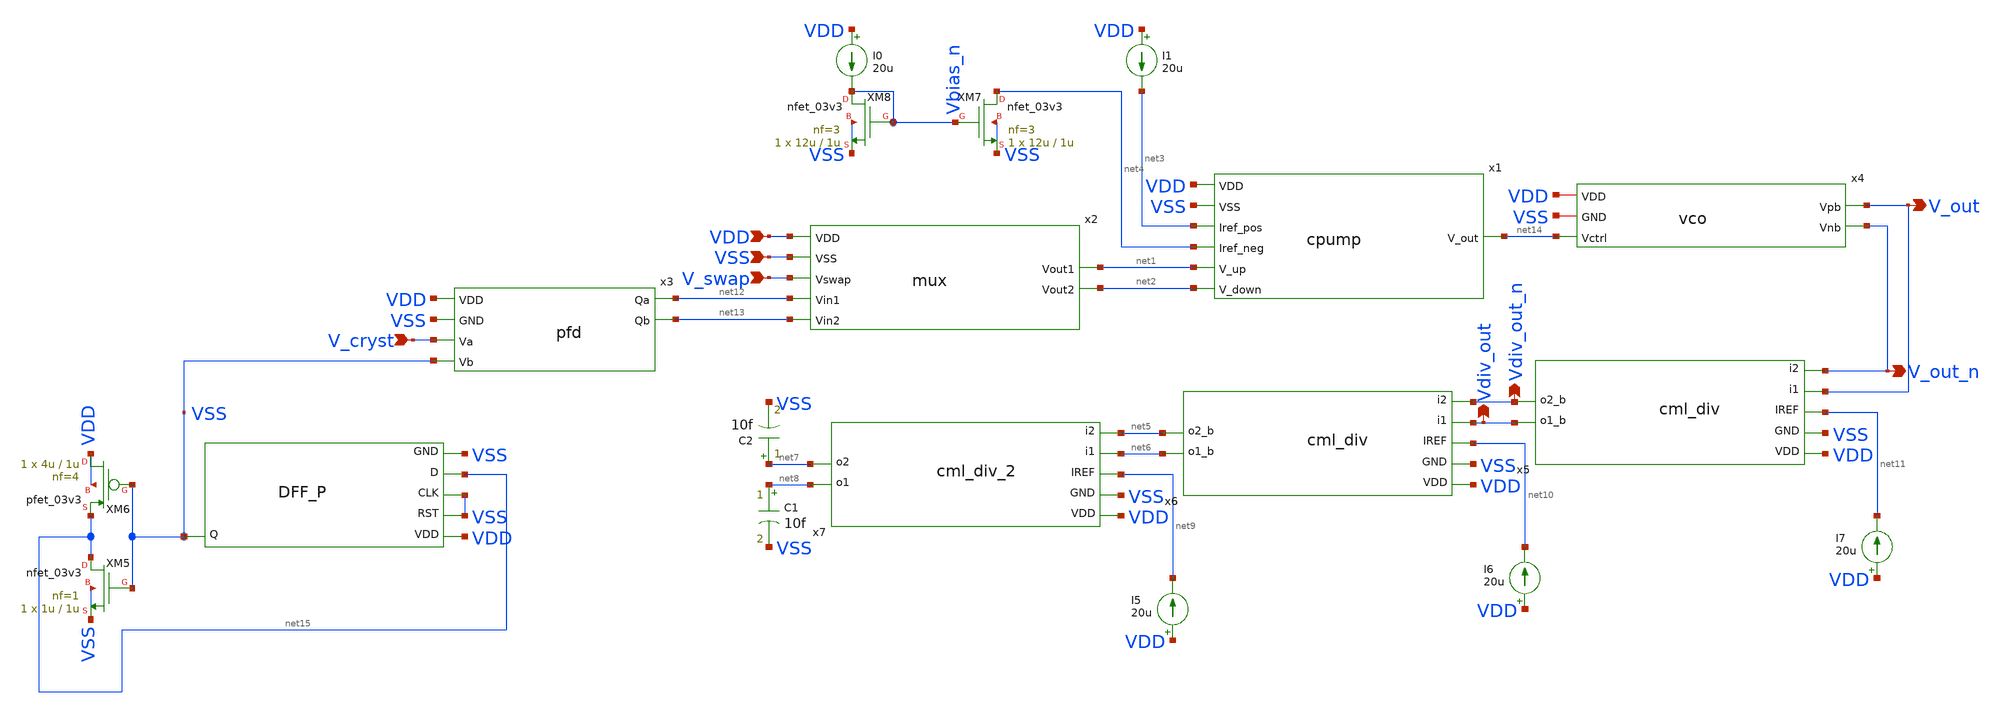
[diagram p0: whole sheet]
** sch_path: blocks/pll/pll.sch
**.subckt pll VDD VSS V_swap V_cryst V_out V_out_n Vdiv_out_n Vdiv_out
*.ipin VDD
*.ipin VSS
*.ipin V_swap
*.ipin V_cryst
*.opin V_out
*.opin V_out_n
*.opin Vdiv_out_n
*.opin Vdiv_out
x1 net3 VDD net1 net14 net2 VSS net4 cpump
x2 net2 net13 VDD V_swap VSS net1 net12 mux
x3 VDD VSS V_cryst net12 VSS net13 pfd
x4 V_out_n V_out net14 VDD VSS vco
x5 VDD VSS Vdiv_out Vdiv_out_n V_out_n V_out net11 cml_div
x6 VDD VSS net6 net5 Vdiv_out_n Vdiv_out net10 cml_div
XM7 net4 Vbias_n VSS VSS nfet_03v3 L=1u W=12u nf=3 ad='int((nf+1)/2) * W/nf * 0.18u' as='int((nf+2)/2) * W/nf * 0.18u'
+ pd='2*int((nf+1)/2) * (W/nf + 0.18u)' ps='2*int((nf+2)/2) * (W/nf + 0.18u)' nrd='0.18u / W' nrs='0.18u / W'
+ sa=0 sb=0 sd=0 m=1
XM8 Vbias_n Vbias_n VSS VSS nfet_03v3 L=1u W=12u nf=3 ad='int((nf+1)/2) * W/nf * 0.18u' as='int((nf+2)/2) * W/nf * 0.18u'
+ pd='2*int((nf+1)/2) * (W/nf + 0.18u)' ps='2*int((nf+2)/2) * (W/nf + 0.18u)' nrd='0.18u / W' nrs='0.18u / W'
+ sa=0 sb=0 sd=0 m=1
I0 VDD Vbias_n 20u
I1 VDD net3 20u
I5 VDD net9 20u
I6 VDD net10 20u
I7 VDD net11 20u
x8 VDD VSS VSS net15 VSS VSS dff_encoder
XM5 net15 VSS VSS VSS nfet_03v3 L=1u W=1u nf=1 ad='int((nf+1)/2) * W/nf * 0.18u' as='int((nf+2)/2) * W/nf * 0.18u'
+ pd='2*int((nf+1)/2) * (W/nf + 0.18u)' ps='2*int((nf+2)/2) * (W/nf + 0.18u)' nrd='0.18u / W' nrs='0.18u / W'
+ sa=0 sb=0 sd=0 m=1
XM6 VDD VSS net15 VDD pfet_03v3 L=1u W=4u nf=4 ad='int((nf+1)/2) * W/nf * 0.18u' as='int((nf+2)/2) * W/nf * 0.18u'
+ pd='2*int((nf+1)/2) * (W/nf + 0.18u)' ps='2*int((nf+2)/2) * (W/nf + 0.18u)' nrd='0.18u / W' nrs='0.18u / W'
+ sa=0 sb=0 sd=0 m=1
x7 VDD VSS net8 net7 net5 net6 net9 cml_div_2
C1 net8 VSS 10f m=1
C2 net7 VSS 10f m=1
**** begin user architecture code

.include /foss/pdks/gf180mcuD/libs.tech/ngspice/design.ngspice
.lib /foss/pdks/gf180mcuD/libs.tech/ngspice/sm141064.ngspice typical
.lib /foss/pdks/gf180mcuD/libs.tech/ngspice/sm141064.ngspice bjt_typical
.lib /foss/pdks/gf180mcuD/libs.tech/ngspice/sm141064.ngspice diode_typical
.lib /foss/pdks/gf180mcuD/libs.tech/ngspice/sm141064.ngspice res_typical
.lib /foss/pdks/gf180mcuD/libs.tech/ngspice/sm141064.ngspice mimcap_typical
.lib /foss/pdks/gf180mcuD/libs.tech/ngspice/sm141064.ngspice moscap_typical

.option method = gear

V_VDD   VDD     0 DC 3.3
V_VSS   VSS     0 DC 0
V_SWP   V_swap  0 DC 0
V_CRYST V_cryst 0 SIN(1.65 1.65 50meg 0 0 0)

.control
    set temp = 25

    let freq = 50meg
    let pers = 500
    let persteps = 20

    let tper = 1 / freq
    let tfin = tper * pers
    let tstep = tper / persteps
    let tplotst = tfin - 2 * tper

    tran 10ps 100ns
    write pll_toplevel.raw

    plot V_out xlimit $&tplotst $&tfin
.endc


**** end user architecture code
**.ends

* expanding   symbol:  blocks/pll/cpump.sym # of pins=7
** sym_path: blocks/pll/cpump.sym
** sch_path: blocks/pll/cpump.sch
.subckt cpump Iref_pos VDD V_up V_out V_down VSS Iref_neg
*.ipin Iref_pos
*.ipin Iref_neg
*.ipin V_up
*.ipin V_down
*.iopin VDD
*.iopin VSS
*.opin V_out
XM1 V_out V_up Iref_pos VDD pfet_03v3 L=1u W=40u nf=10 ad='int((nf+1)/2) * W/nf * 0.18u' as='int((nf+2)/2) * W/nf * 0.18u'
+ pd='2*int((nf+1)/2) * (W/nf + 0.18u)' ps='2*int((nf+2)/2) * (W/nf + 0.18u)' nrd='0.18u / W' nrs='0.18u / W'
+ sa=0 sb=0 sd=0 m=1
XM2 V_out V_down Iref_neg VSS nfet_03v3 L=1u W=4u nf=1 ad='int((nf+1)/2) * W/nf * 0.18u' as='int((nf+2)/2) * W/nf * 0.18u'
+ pd='2*int((nf+1)/2) * (W/nf + 0.18u)' ps='2*int((nf+2)/2) * (W/nf + 0.18u)' nrd='0.18u / W' nrs='0.18u / W'
+ sa=0 sb=0 sd=0 m=1
XR1 net1 V_out VSS ppolyf_u r_width=2e-6 r_length=8e-6 m=1
XC1 net1 VSS cap_mim_2f0_m4m5_noshield c_width=5e-6 c_length=5e-6 m=1
XC2 V_out VSS cap_mim_2f0_m4m5_noshield c_width=5e-6 c_length=5e-6 m=1
.ends


* expanding   symbol:  blocks/pll/mux.sym # of pins=7
** sym_path: blocks/pll/mux.sym
** sch_path: blocks/pll/mux.sch
.subckt mux Vout2 Vin2 VDD Vswap VSS Vout1 Vin1
*.ipin Vin1
*.opin Vout1
*.ipin Vin2
*.opin Vout2
*.iopin VDD
*.iopin VSS
*.ipin Vswap
XM1 Vout1 net1 Vin2 VSS nfet_03v3 L=1u W=4u nf=1 ad='int((nf+1)/2) * W/nf * 0.18u' as='int((nf+2)/2) * W/nf * 0.18u'
+ pd='2*int((nf+1)/2) * (W/nf + 0.18u)' ps='2*int((nf+2)/2) * (W/nf + 0.18u)' nrd='0.18u / W' nrs='0.18u / W'
+ sa=0 sb=0 sd=0 m=1
XM2 Vout1 Vswap Vin2 VDD pfet_03v3 L=1u W=16u nf=4 ad='int((nf+1)/2) * W/nf * 0.18u' as='int((nf+2)/2) * W/nf * 0.18u'
+ pd='2*int((nf+1)/2) * (W/nf + 0.18u)' ps='2*int((nf+2)/2) * (W/nf + 0.18u)' nrd='0.18u / W' nrs='0.18u / W'
+ sa=0 sb=0 sd=0 m=1
XM3 Vout2 Vswap Vin1 VSS nfet_03v3 L=1u W=4u nf=1 ad='int((nf+1)/2) * W/nf * 0.18u' as='int((nf+2)/2) * W/nf * 0.18u'
+ pd='2*int((nf+1)/2) * (W/nf + 0.18u)' ps='2*int((nf+2)/2) * (W/nf + 0.18u)' nrd='0.18u / W' nrs='0.18u / W'
+ sa=0 sb=0 sd=0 m=1
XM4 Vout2 net1 Vin1 VDD pfet_03v3 L=1u W=16u nf=4 ad='int((nf+1)/2) * W/nf * 0.18u' as='int((nf+2)/2) * W/nf * 0.18u'
+ pd='2*int((nf+1)/2) * (W/nf + 0.18u)' ps='2*int((nf+2)/2) * (W/nf + 0.18u)' nrd='0.18u / W' nrs='0.18u / W'
+ sa=0 sb=0 sd=0 m=1
XM5 net1 Vswap VSS VSS nfet_03v3 L=1u W=1u nf=1 ad='int((nf+1)/2) * W/nf * 0.18u' as='int((nf+2)/2) * W/nf * 0.18u'
+ pd='2*int((nf+1)/2) * (W/nf + 0.18u)' ps='2*int((nf+2)/2) * (W/nf + 0.18u)' nrd='0.18u / W' nrs='0.18u / W'
+ sa=0 sb=0 sd=0 m=1
XM6 VDD Vswap net1 VDD pfet_03v3 L=1u W=4u nf=4 ad='int((nf+1)/2) * W/nf * 0.18u' as='int((nf+2)/2) * W/nf * 0.18u'
+ pd='2*int((nf+1)/2) * (W/nf + 0.18u)' ps='2*int((nf+2)/2) * (W/nf + 0.18u)' nrd='0.18u / W' nrs='0.18u / W'
+ sa=0 sb=0 sd=0 m=1
XM7 Vout2 net1 Vin2 VSS nfet_03v3 L=1u W=4u nf=1 ad='int((nf+1)/2) * W/nf * 0.18u' as='int((nf+2)/2) * W/nf * 0.18u'
+ pd='2*int((nf+1)/2) * (W/nf + 0.18u)' ps='2*int((nf+2)/2) * (W/nf + 0.18u)' nrd='0.18u / W' nrs='0.18u / W'
+ sa=0 sb=0 sd=0 m=1
XM8 Vout2 Vswap Vin2 VDD pfet_03v3 L=1u W=16u nf=4 ad='int((nf+1)/2) * W/nf * 0.18u' as='int((nf+2)/2) * W/nf * 0.18u'
+ pd='2*int((nf+1)/2) * (W/nf + 0.18u)' ps='2*int((nf+2)/2) * (W/nf + 0.18u)' nrd='0.18u / W' nrs='0.18u / W'
+ sa=0 sb=0 sd=0 m=1
XM9 Vout1 Vswap Vin1 VSS nfet_03v3 L=1u W=4u nf=1 ad='int((nf+1)/2) * W/nf * 0.18u' as='int((nf+2)/2) * W/nf * 0.18u'
+ pd='2*int((nf+1)/2) * (W/nf + 0.18u)' ps='2*int((nf+2)/2) * (W/nf + 0.18u)' nrd='0.18u / W' nrs='0.18u / W'
+ sa=0 sb=0 sd=0 m=1
XM10 Vout1 net1 Vin1 VDD pfet_03v3 L=1u W=16u nf=4 ad='int((nf+1)/2) * W/nf * 0.18u' as='int((nf+2)/2) * W/nf * 0.18u'
+ pd='2*int((nf+1)/2) * (W/nf + 0.18u)' ps='2*int((nf+2)/2) * (W/nf + 0.18u)' nrd='0.18u / W' nrs='0.18u / W'
+ sa=0 sb=0 sd=0 m=1
.ends


* expanding   symbol:  blocks/pll/pfd.sym # of pins=6
** sym_path: pll_block_templates_v1/layout2/pfd.sym
** sch_path: pll_block_templates_v1/layout2/pfd.sch
.subckt pfd VDD GND Va Qa Vb Qb
*.ipin Vb
*.ipin Va
*.opin Qa
*.opin Qb
*.iopin VDD
*.iopin GND
x2 VDD Va Qa net1 GND nor
x3 VDD net1 net2 Qa GND nor
x4 VDD net1 net3 net2 GND nor
x5 VDD net2 RST net3 GND nor
x1 VDD Vb Qb net4 GND nor
x6 VDD net4 net5 Qb GND nor
x7 VDD net4 net6 net5 GND nor
x8 VDD net5 RST net6 GND nor
x9 VDD net7 Qa Qb GND nand
XM1 RST net7 GND GND nfet_03v3 L=0.28u W=0.22u nf=1 ad='int((nf+1)/2) * W/nf * 0.18u' as='int((nf+2)/2) * W/nf * 0.18u'
+ pd='2*int((nf+1)/2) * (W/nf + 0.18u)' ps='2*int((nf+2)/2) * (W/nf + 0.18u)' nrd='0.18u / W' nrs='0.18u / W'
+ sa=0 sb=0 sd=0 m=1
XM2 RST net7 VDD VDD pfet_03v3 L=0.28u W=0.22u nf=1 ad='int((nf+1)/2) * W/nf * 0.18u' as='int((nf+2)/2) * W/nf * 0.18u'
+ pd='2*int((nf+1)/2) * (W/nf + 0.18u)' ps='2*int((nf+2)/2) * (W/nf + 0.18u)' nrd='0.18u / W' nrs='0.18u / W'
+ sa=0 sb=0 sd=0 m=1
.ends


* expanding   symbol:  blocks/pll/vco.sym # of pins=5
** sym_path: blocks/pll/vco.sym
** sch_path: blocks/pll/vco.sch
.subckt vco Vnb Vpb Vctrl VDD GND
*.iopin VDD
*.iopin GND
*.ipin Vctrl
*.opin Vpb
*.opin Vnb
XM1 Vn Vp net3 GND nfet_03v3 L=0.28u W=40u nf=10 ad='int((nf+1)/2) * W/nf * 0.18u' as='int((nf+2)/2) * W/nf * 0.18u'
+ pd='2*int((nf+1)/2) * (W/nf + 0.18u)' ps='2*int((nf+2)/2) * (W/nf + 0.18u)' nrd='0.18u / W' nrs='0.18u / W'
+ sa=0 sb=0 sd=0 m=1
XM2 Vp Vn net2 GND nfet_03v3 L=0.28u W=40u nf=10 ad='int((nf+1)/2) * W/nf * 0.18u' as='int((nf+2)/2) * W/nf * 0.18u'
+ pd='2*int((nf+1)/2) * (W/nf + 0.18u)' ps='2*int((nf+2)/2) * (W/nf + 0.18u)' nrd='0.18u / W' nrs='0.18u / W'
+ sa=0 sb=0 sd=0 m=1
XM3 net2 Vn GND GND nfet_03v3 L=0.28u W=15u nf=3 ad='int((nf+1)/2) * W/nf * 0.18u' as='int((nf+2)/2) * W/nf * 0.18u'
+ pd='2*int((nf+1)/2) * (W/nf + 0.18u)' ps='2*int((nf+2)/2) * (W/nf + 0.18u)' nrd='0.18u / W' nrs='0.18u / W'
+ sa=0 sb=0 sd=0 m=1
XM4 net3 Vp GND GND nfet_03v3 L=0.28u W=15u nf=3 ad='int((nf+1)/2) * W/nf * 0.18u' as='int((nf+2)/2) * W/nf * 0.18u'
+ pd='2*int((nf+1)/2) * (W/nf + 0.18u)' ps='2*int((nf+2)/2) * (W/nf + 0.18u)' nrd='0.18u / W' nrs='0.18u / W'
+ sa=0 sb=0 sd=0 m=1
XR1 net1 Vctrl GND pplus_u r_width=5e-6 r_length=20e-6 m=1
XM5 Vn Vp VDD VDD pfet_03v3 L=0.28u W=40u nf=10 ad='int((nf+1)/2) * W/nf * 0.18u' as='int((nf+2)/2) * W/nf * 0.18u'
+ pd='2*int((nf+1)/2) * (W/nf + 0.18u)' ps='2*int((nf+2)/2) * (W/nf + 0.18u)' nrd='0.18u / W' nrs='0.18u / W'
+ sa=0 sb=0 sd=0 m=1
XM6 Vp Vn VDD VDD pfet_03v3 L=0.28u W=40u nf=10 ad='int((nf+1)/2) * W/nf * 0.18u' as='int((nf+2)/2) * W/nf * 0.18u'
+ pd='2*int((nf+1)/2) * (W/nf + 0.18u)' ps='2*int((nf+2)/2) * (W/nf + 0.18u)' nrd='0.18u / W' nrs='0.18u / W'
+ sa=0 sb=0 sd=0 m=1
L9 Vn Vp 340p m=1
XM7 Vp net1 Vp Vp nfet_03v3 L=20u W=44u nf=2 ad='int((nf+1)/2) * W/nf * 0.18u' as='int((nf+2)/2) * W/nf * 0.18u'
+ pd='2*int((nf+1)/2) * (W/nf + 0.18u)' ps='2*int((nf+2)/2) * (W/nf + 0.18u)' nrd='0.18u / W' nrs='0.18u / W'
+ sa=0 sb=0 sd=0 m=2
XM8 Vn net1 Vn Vn nfet_03v3 L=20u W=44u nf=2 ad='int((nf+1)/2) * W/nf * 0.18u' as='int((nf+2)/2) * W/nf * 0.18u'
+ pd='2*int((nf+1)/2) * (W/nf + 0.18u)' ps='2*int((nf+2)/2) * (W/nf + 0.18u)' nrd='0.18u / W' nrs='0.18u / W'
+ sa=0 sb=0 sd=0 m=2
XM9 VDD Vp Vnb GND nfet_03v3 L=0.28u W=29.995u nf=7 ad='int((nf+1)/2) * W/nf * 0.18u' as='int((nf+2)/2) * W/nf * 0.18u'
+ pd='2*int((nf+1)/2) * (W/nf + 0.18u)' ps='2*int((nf+2)/2) * (W/nf + 0.18u)' nrd='0.18u / W' nrs='0.18u / W'
+ sa=0 sb=0 sd=0 m=1
XR3 Vnb GND GND pplus_u r_width=5e-6 r_length=20e-6 m=1
XM10 VDD Vn Vpb GND nfet_03v3 L=0.28u W=29.995u nf=7 ad='int((nf+1)/2) * W/nf * 0.18u' as='int((nf+2)/2) * W/nf * 0.18u'
+ pd='2*int((nf+1)/2) * (W/nf + 0.18u)' ps='2*int((nf+2)/2) * (W/nf + 0.18u)' nrd='0.18u / W' nrs='0.18u / W'
+ sa=0 sb=0 sd=0 m=1
XR4 Vpb GND GND pplus_u r_width=5e-6 r_length=20e-6 m=1
XC5 net3 Vn cap_mim_2f0_m4m5_noshield c_width=5e-6 c_length=5e-6 m=1
XC2 net3 GND cap_mim_2f0_m4m5_noshield c_width=5e-6 c_length=5e-6 m=1
XC3 net2 GND cap_mim_2f0_m4m5_noshield c_width=5e-6 c_length=5e-6 m=1
XC1 net2 Vp cap_mim_2f0_m4m5_noshield c_width=5e-6 c_length=5e-6 m=1
.ends


* expanding   symbol:  blocks/pll/cml_div.sym # of pins=7
** sym_path: blocks/pll/cml_div.sym
** sch_path: blocks/pll/cml_div.sch
.subckt cml_div VDD GND o1_b o2_b i2 i1 IREF
*.ipin i2
*.ipin i1
*.opin o2_b
*.opin o1_b
*.iopin VDD
*.iopin GND
*.ipin IREF
XM1 o1 o3 net1 GND nfet_03v3 L=0.28u W=1.44u nf=1 ad='int((nf+1)/2) * W/nf * 0.18u' as='int((nf+2)/2) * W/nf * 0.18u'
+ pd='2*int((nf+1)/2) * (W/nf + 0.18u)' ps='2*int((nf+2)/2) * (W/nf + 0.18u)' nrd='0.18u / W' nrs='0.18u / W'
+ sa=0 sb=0 sd=0 m=1
XM2 o2 o4 net1 GND nfet_03v3 L=0.28u W=1.44u nf=1 ad='int((nf+1)/2) * W/nf * 0.18u' as='int((nf+2)/2) * W/nf * 0.18u'
+ pd='2*int((nf+1)/2) * (W/nf + 0.18u)' ps='2*int((nf+2)/2) * (W/nf + 0.18u)' nrd='0.18u / W' nrs='0.18u / W'
+ sa=0 sb=0 sd=0 m=1
XM3 o1 o1 VDD VDD pfet_03v3 L=0.28u W=1.22u nf=1 ad='int((nf+1)/2) * W/nf * 0.18u' as='int((nf+2)/2) * W/nf * 0.18u'
+ pd='2*int((nf+1)/2) * (W/nf + 0.18u)' ps='2*int((nf+2)/2) * (W/nf + 0.18u)' nrd='0.18u / W' nrs='0.18u / W'
+ sa=0 sb=0 sd=0 m=1
XM4 net3 IREF GND GND nfet_03v3 L=0.28u W=18.3u nf=15 ad='int((nf+1)/2) * W/nf * 0.18u' as='int((nf+2)/2) * W/nf * 0.18u'
+ pd='2*int((nf+1)/2) * (W/nf + 0.18u)' ps='2*int((nf+2)/2) * (W/nf + 0.18u)' nrd='0.18u / W' nrs='0.18u / W'
+ sa=0 sb=0 sd=0 m=1
XM5 o2 o2 VDD VDD pfet_03v3 L=0.28u W=1.22u nf=1 ad='int((nf+1)/2) * W/nf * 0.18u' as='int((nf+2)/2) * W/nf * 0.18u'
+ pd='2*int((nf+1)/2) * (W/nf + 0.18u)' ps='2*int((nf+2)/2) * (W/nf + 0.18u)' nrd='0.18u / W' nrs='0.18u / W'
+ sa=0 sb=0 sd=0 m=1
XM6 net1 i1 net3 GND nfet_03v3 L=0.28u W=4.5u nf=3 ad='int((nf+1)/2) * W/nf * 0.18u' as='int((nf+2)/2) * W/nf * 0.18u'
+ pd='2*int((nf+1)/2) * (W/nf + 0.18u)' ps='2*int((nf+2)/2) * (W/nf + 0.18u)' nrd='0.18u / W' nrs='0.18u / W'
+ sa=0 sb=0 sd=0 m=1
XM7 o1 o2 net2 GND nfet_03v3 L=0.28u W=1.44u nf=2 ad='int((nf+1)/2) * W/nf * 0.18u' as='int((nf+2)/2) * W/nf * 0.18u'
+ pd='2*int((nf+1)/2) * (W/nf + 0.18u)' ps='2*int((nf+2)/2) * (W/nf + 0.18u)' nrd='0.18u / W' nrs='0.18u / W'
+ sa=0 sb=0 sd=0 m=1
XM8 o2 o1 net2 GND nfet_03v3 L=0.28u W=1.44u nf=2 ad='int((nf+1)/2) * W/nf * 0.18u' as='int((nf+2)/2) * W/nf * 0.18u'
+ pd='2*int((nf+1)/2) * (W/nf + 0.18u)' ps='2*int((nf+2)/2) * (W/nf + 0.18u)' nrd='0.18u / W' nrs='0.18u / W'
+ sa=0 sb=0 sd=0 m=1
XM11 net2 i2 net3 GND nfet_03v3 L=0.28u W=4.5u nf=3 ad='int((nf+1)/2) * W/nf * 0.18u' as='int((nf+2)/2) * W/nf * 0.18u'
+ pd='2*int((nf+1)/2) * (W/nf + 0.18u)' ps='2*int((nf+2)/2) * (W/nf + 0.18u)' nrd='0.18u / W' nrs='0.18u / W'
+ sa=0 sb=0 sd=0 m=1
XM9 IREF IREF GND GND nfet_03v3 L=0.28u W=0.61u nf=1 ad='int((nf+1)/2) * W/nf * 0.18u' as='int((nf+2)/2) * W/nf * 0.18u'
+ pd='2*int((nf+1)/2) * (W/nf + 0.18u)' ps='2*int((nf+2)/2) * (W/nf + 0.18u)' nrd='0.18u / W' nrs='0.18u / W'
+ sa=0 sb=0 sd=0 m=1
XM20 o3 o2 net4 GND nfet_03v3 L=0.28u W=1.44u nf=1 ad='int((nf+1)/2) * W/nf * 0.18u' as='int((nf+2)/2) * W/nf * 0.18u'
+ pd='2*int((nf+1)/2) * (W/nf + 0.18u)' ps='2*int((nf+2)/2) * (W/nf + 0.18u)' nrd='0.18u / W' nrs='0.18u / W'
+ sa=0 sb=0 sd=0 m=1
XM21 o4 o1 net4 GND nfet_03v3 L=0.28u W=1.44u nf=1 ad='int((nf+1)/2) * W/nf * 0.18u' as='int((nf+2)/2) * W/nf * 0.18u'
+ pd='2*int((nf+1)/2) * (W/nf + 0.18u)' ps='2*int((nf+2)/2) * (W/nf + 0.18u)' nrd='0.18u / W' nrs='0.18u / W'
+ sa=0 sb=0 sd=0 m=1
XM22 o3 o3 VDD VDD pfet_03v3 L=0.28u W=1.22u nf=1 ad='int((nf+1)/2) * W/nf * 0.18u' as='int((nf+2)/2) * W/nf * 0.18u'
+ pd='2*int((nf+1)/2) * (W/nf + 0.18u)' ps='2*int((nf+2)/2) * (W/nf + 0.18u)' nrd='0.18u / W' nrs='0.18u / W'
+ sa=0 sb=0 sd=0 m=1
XM24 o4 o4 VDD VDD pfet_03v3 L=0.28u W=1.22u nf=1 ad='int((nf+1)/2) * W/nf * 0.18u' as='int((nf+2)/2) * W/nf * 0.18u'
+ pd='2*int((nf+1)/2) * (W/nf + 0.18u)' ps='2*int((nf+2)/2) * (W/nf + 0.18u)' nrd='0.18u / W' nrs='0.18u / W'
+ sa=0 sb=0 sd=0 m=1
XM25 net4 i2 net6 GND nfet_03v3 L=0.28u W=4.5u nf=3 ad='int((nf+1)/2) * W/nf * 0.18u' as='int((nf+2)/2) * W/nf * 0.18u'
+ pd='2*int((nf+1)/2) * (W/nf + 0.18u)' ps='2*int((nf+2)/2) * (W/nf + 0.18u)' nrd='0.18u / W' nrs='0.18u / W'
+ sa=0 sb=0 sd=0 m=1
XM26 o3 o4 net5 GND nfet_03v3 L=0.28u W=1.44u nf=2 ad='int((nf+1)/2) * W/nf * 0.18u' as='int((nf+2)/2) * W/nf * 0.18u'
+ pd='2*int((nf+1)/2) * (W/nf + 0.18u)' ps='2*int((nf+2)/2) * (W/nf + 0.18u)' nrd='0.18u / W' nrs='0.18u / W'
+ sa=0 sb=0 sd=0 m=1
XM27 o4 o3 net5 GND nfet_03v3 L=0.28u W=1.44u nf=2 ad='int((nf+1)/2) * W/nf * 0.18u' as='int((nf+2)/2) * W/nf * 0.18u'
+ pd='2*int((nf+1)/2) * (W/nf + 0.18u)' ps='2*int((nf+2)/2) * (W/nf + 0.18u)' nrd='0.18u / W' nrs='0.18u / W'
+ sa=0 sb=0 sd=0 m=1
XM28 net5 i1 net6 GND nfet_03v3 L=0.28u W=4.5u nf=3 ad='int((nf+1)/2) * W/nf * 0.18u' as='int((nf+2)/2) * W/nf * 0.18u'
+ pd='2*int((nf+1)/2) * (W/nf + 0.18u)' ps='2*int((nf+2)/2) * (W/nf + 0.18u)' nrd='0.18u / W' nrs='0.18u / W'
+ sa=0 sb=0 sd=0 m=1
XM10 net6 IREF GND GND nfet_03v3 L=0.28u W=18.3u nf=15 ad='int((nf+1)/2) * W/nf * 0.18u' as='int((nf+2)/2) * W/nf * 0.18u'
+ pd='2*int((nf+1)/2) * (W/nf + 0.18u)' ps='2*int((nf+2)/2) * (W/nf + 0.18u)' nrd='0.18u / W' nrs='0.18u / W'
+ sa=0 sb=0 sd=0 m=1
XM12 VDD o2 o2_b GND nfet_03v3 L=0.28u W=7.5u nf=5 ad='int((nf+1)/2) * W/nf * 0.18u' as='int((nf+2)/2) * W/nf * 0.18u'
+ pd='2*int((nf+1)/2) * (W/nf + 0.18u)' ps='2*int((nf+2)/2) * (W/nf + 0.18u)' nrd='0.18u / W' nrs='0.18u / W'
+ sa=0 sb=0 sd=0 m=1
XR1 GND o2_b GND ppolyf_u_1k r_width=2e-6 r_length=16e-6 m=1
XM13 VDD o1 o1_b GND nfet_03v3 L=0.28u W=7.5u nf=5 ad='int((nf+1)/2) * W/nf * 0.18u' as='int((nf+2)/2) * W/nf * 0.18u'
+ pd='2*int((nf+1)/2) * (W/nf + 0.18u)' ps='2*int((nf+2)/2) * (W/nf + 0.18u)' nrd='0.18u / W' nrs='0.18u / W'
+ sa=0 sb=0 sd=0 m=1
XR2 GND o1_b GND ppolyf_u_1k r_width=2e-6 r_length=16e-6 m=1
.ends


* expanding   symbol:  blocks/pll/cml_div_2.sym # of pins=7
** sym_path: blocks/pll/cml_div_2.sym
** sch_path: blocks/pll/cml_div_2.sch
.subckt cml_div_2 VDD GND o1 o2 i2 i1 IREF
*.ipin i2
*.ipin i1
*.opin o2
*.opin o1
*.iopin VDD
*.iopin GND
*.ipin IREF
XM1 o1 o3 net1 GND nfet_03v3 L=0.28u W=1.44u nf=1 ad='int((nf+1)/2) * W/nf * 0.18u' as='int((nf+2)/2) * W/nf * 0.18u'
+ pd='2*int((nf+1)/2) * (W/nf + 0.18u)' ps='2*int((nf+2)/2) * (W/nf + 0.18u)' nrd='0.18u / W' nrs='0.18u / W'
+ sa=0 sb=0 sd=0 m=1
XM2 o2 o4 net1 GND nfet_03v3 L=0.28u W=1.44u nf=1 ad='int((nf+1)/2) * W/nf * 0.18u' as='int((nf+2)/2) * W/nf * 0.18u'
+ pd='2*int((nf+1)/2) * (W/nf + 0.18u)' ps='2*int((nf+2)/2) * (W/nf + 0.18u)' nrd='0.18u / W' nrs='0.18u / W'
+ sa=0 sb=0 sd=0 m=1
XM4 net3 IREF GND GND nfet_03v3 L=0.28u W=3.66u nf=6 ad='int((nf+1)/2) * W/nf * 0.18u' as='int((nf+2)/2) * W/nf * 0.18u'
+ pd='2*int((nf+1)/2) * (W/nf + 0.18u)' ps='2*int((nf+2)/2) * (W/nf + 0.18u)' nrd='0.18u / W' nrs='0.18u / W'
+ sa=0 sb=0 sd=0 m=1
XM6 net1 i1 net3 GND nfet_03v3 L=0.28u W=4.5u nf=3 ad='int((nf+1)/2) * W/nf * 0.18u' as='int((nf+2)/2) * W/nf * 0.18u'
+ pd='2*int((nf+1)/2) * (W/nf + 0.18u)' ps='2*int((nf+2)/2) * (W/nf + 0.18u)' nrd='0.18u / W' nrs='0.18u / W'
+ sa=0 sb=0 sd=0 m=1
XM7 o1 o2 net2 GND nfet_03v3 L=0.28u W=1.44u nf=2 ad='int((nf+1)/2) * W/nf * 0.18u' as='int((nf+2)/2) * W/nf * 0.18u'
+ pd='2*int((nf+1)/2) * (W/nf + 0.18u)' ps='2*int((nf+2)/2) * (W/nf + 0.18u)' nrd='0.18u / W' nrs='0.18u / W'
+ sa=0 sb=0 sd=0 m=1
XM8 o2 o1 net2 GND nfet_03v3 L=0.28u W=1.44u nf=2 ad='int((nf+1)/2) * W/nf * 0.18u' as='int((nf+2)/2) * W/nf * 0.18u'
+ pd='2*int((nf+1)/2) * (W/nf + 0.18u)' ps='2*int((nf+2)/2) * (W/nf + 0.18u)' nrd='0.18u / W' nrs='0.18u / W'
+ sa=0 sb=0 sd=0 m=1
XM11 net2 i2 net3 GND nfet_03v3 L=0.28u W=4.5u nf=3 ad='int((nf+1)/2) * W/nf * 0.18u' as='int((nf+2)/2) * W/nf * 0.18u'
+ pd='2*int((nf+1)/2) * (W/nf + 0.18u)' ps='2*int((nf+2)/2) * (W/nf + 0.18u)' nrd='0.18u / W' nrs='0.18u / W'
+ sa=0 sb=0 sd=0 m=1
XM9 IREF IREF GND GND nfet_03v3 L=0.28u W=0.61u nf=1 ad='int((nf+1)/2) * W/nf * 0.18u' as='int((nf+2)/2) * W/nf * 0.18u'
+ pd='2*int((nf+1)/2) * (W/nf + 0.18u)' ps='2*int((nf+2)/2) * (W/nf + 0.18u)' nrd='0.18u / W' nrs='0.18u / W'
+ sa=0 sb=0 sd=0 m=1
XM20 o3 o2 net4 GND nfet_03v3 L=0.28u W=1.44u nf=1 ad='int((nf+1)/2) * W/nf * 0.18u' as='int((nf+2)/2) * W/nf * 0.18u'
+ pd='2*int((nf+1)/2) * (W/nf + 0.18u)' ps='2*int((nf+2)/2) * (W/nf + 0.18u)' nrd='0.18u / W' nrs='0.18u / W'
+ sa=0 sb=0 sd=0 m=1
XM21 o4 o1 net4 GND nfet_03v3 L=0.28u W=1.44u nf=1 ad='int((nf+1)/2) * W/nf * 0.18u' as='int((nf+2)/2) * W/nf * 0.18u'
+ pd='2*int((nf+1)/2) * (W/nf + 0.18u)' ps='2*int((nf+2)/2) * (W/nf + 0.18u)' nrd='0.18u / W' nrs='0.18u / W'
+ sa=0 sb=0 sd=0 m=1
XM25 net4 i2 net6 GND nfet_03v3 L=0.28u W=4.5u nf=3 ad='int((nf+1)/2) * W/nf * 0.18u' as='int((nf+2)/2) * W/nf * 0.18u'
+ pd='2*int((nf+1)/2) * (W/nf + 0.18u)' ps='2*int((nf+2)/2) * (W/nf + 0.18u)' nrd='0.18u / W' nrs='0.18u / W'
+ sa=0 sb=0 sd=0 m=1
XM26 o3 o4 net5 GND nfet_03v3 L=0.28u W=1.44u nf=2 ad='int((nf+1)/2) * W/nf * 0.18u' as='int((nf+2)/2) * W/nf * 0.18u'
+ pd='2*int((nf+1)/2) * (W/nf + 0.18u)' ps='2*int((nf+2)/2) * (W/nf + 0.18u)' nrd='0.18u / W' nrs='0.18u / W'
+ sa=0 sb=0 sd=0 m=1
XM27 o4 o3 net5 GND nfet_03v3 L=0.28u W=1.44u nf=2 ad='int((nf+1)/2) * W/nf * 0.18u' as='int((nf+2)/2) * W/nf * 0.18u'
+ pd='2*int((nf+1)/2) * (W/nf + 0.18u)' ps='2*int((nf+2)/2) * (W/nf + 0.18u)' nrd='0.18u / W' nrs='0.18u / W'
+ sa=0 sb=0 sd=0 m=1
XM28 net5 i1 net6 GND nfet_03v3 L=0.28u W=4.5u nf=3 ad='int((nf+1)/2) * W/nf * 0.18u' as='int((nf+2)/2) * W/nf * 0.18u'
+ pd='2*int((nf+1)/2) * (W/nf + 0.18u)' ps='2*int((nf+2)/2) * (W/nf + 0.18u)' nrd='0.18u / W' nrs='0.18u / W'
+ sa=0 sb=0 sd=0 m=1
XM10 net6 IREF GND GND nfet_03v3 L=0.28u W=3.66u nf=6 ad='int((nf+1)/2) * W/nf * 0.18u' as='int((nf+2)/2) * W/nf * 0.18u'
+ pd='2*int((nf+1)/2) * (W/nf + 0.18u)' ps='2*int((nf+2)/2) * (W/nf + 0.18u)' nrd='0.18u / W' nrs='0.18u / W'
+ sa=0 sb=0 sd=0 m=1
XR1 o4 VDD GND ppolyf_u_1k r_width=1e-6 r_length=15e-6 m=1
XR2 o3 VDD GND ppolyf_u_1k r_width=1e-6 r_length=15e-6 m=1
XR3 o2 VDD GND ppolyf_u_1k r_width=1e-6 r_length=15e-6 m=1
XR4 o1 VDD GND ppolyf_u_1k r_width=1e-6 r_length=15e-6 m=1
.ends


* expanding   symbol:  blocks/pll/nor.sym # of pins=5
** sym_path: blocks/pll/nor.sym
** sch_path: blocks/pll/nor.sch
.subckt nor VDD A B Z GND
*.ipin A
*.ipin B
*.opin Z
*.iopin GND
*.iopin VDD
XM1 Z A GND GND nfet_03v3 L=0.28u W=0.22u nf=1 ad='int((nf+1)/2) * W/nf * 0.18u' as='int((nf+2)/2) * W/nf * 0.18u'
+ pd='2*int((nf+1)/2) * (W/nf + 0.18u)' ps='2*int((nf+2)/2) * (W/nf + 0.18u)' nrd='0.18u / W' nrs='0.18u / W'
+ sa=0 sb=0 sd=0 m=1
XM2 Z B net1 VDD pfet_03v3 L=0.28u W=0.22u nf=1 ad='int((nf+1)/2) * W/nf * 0.18u' as='int((nf+2)/2) * W/nf * 0.18u'
+ pd='2*int((nf+1)/2) * (W/nf + 0.18u)' ps='2*int((nf+2)/2) * (W/nf + 0.18u)' nrd='0.18u / W' nrs='0.18u / W'
+ sa=0 sb=0 sd=0 m=1
XM3 Z B GND GND nfet_03v3 L=0.28u W=0.22u nf=1 ad='int((nf+1)/2) * W/nf * 0.18u' as='int((nf+2)/2) * W/nf * 0.18u'
+ pd='2*int((nf+1)/2) * (W/nf + 0.18u)' ps='2*int((nf+2)/2) * (W/nf + 0.18u)' nrd='0.18u / W' nrs='0.18u / W'
+ sa=0 sb=0 sd=0 m=1
XM4 net1 A VDD VDD pfet_03v3 L=0.28u W=0.22u nf=1 ad='int((nf+1)/2) * W/nf * 0.18u' as='int((nf+2)/2) * W/nf * 0.18u'
+ pd='2*int((nf+1)/2) * (W/nf + 0.18u)' ps='2*int((nf+2)/2) * (W/nf + 0.18u)' nrd='0.18u / W' nrs='0.18u / W'
+ sa=0 sb=0 sd=0 m=1
.ends


* expanding   symbol:  blocks/pll/nand.sym # of pins=5
** sym_path: pll_block_templates_v1/layout2/nand.sym
** sch_path: pll_block_templates_v1/layout2/nand.sch
.subckt nand VDD Z A B GND
*.ipin A
*.iopin VDD
*.opin Z
*.iopin GND
*.ipin B
XM1 Z A net1 GND nfet_03v3 L=0.28u W=0.3u nf=1 ad='int((nf+1)/2) * W/nf * 0.18u' as='int((nf+2)/2) * W/nf * 0.18u'
+ pd='2*int((nf+1)/2) * (W/nf + 0.18u)' ps='2*int((nf+2)/2) * (W/nf + 0.18u)' nrd='0.18u / W' nrs='0.18u / W'
+ sa=0 sb=0 sd=0 m=1
XM2 Z A VDD VDD pfet_03v3 L=0.28u W=0.3u nf=1 ad='int((nf+1)/2) * W/nf * 0.18u' as='int((nf+2)/2) * W/nf * 0.18u'
+ pd='2*int((nf+1)/2) * (W/nf + 0.18u)' ps='2*int((nf+2)/2) * (W/nf + 0.18u)' nrd='0.18u / W' nrs='0.18u / W'
+ sa=0 sb=0 sd=0 m=1
XM3 Z B VDD VDD pfet_03v3 L=0.28u W=0.3u nf=1 ad='int((nf+1)/2) * W/nf * 0.18u' as='int((nf+2)/2) * W/nf * 0.18u'
+ pd='2*int((nf+1)/2) * (W/nf + 0.18u)' ps='2*int((nf+2)/2) * (W/nf + 0.18u)' nrd='0.18u / W' nrs='0.18u / W'
+ sa=0 sb=0 sd=0 m=1
XM4 net1 B GND GND nfet_03v3 L=0.28u W=0.3u nf=1 ad='int((nf+1)/2) * W/nf * 0.18u' as='int((nf+2)/2) * W/nf * 0.18u'
+ pd='2*int((nf+1)/2) * (W/nf + 0.18u)' ps='2*int((nf+2)/2) * (W/nf + 0.18u)' nrd='0.18u / W' nrs='0.18u / W'
+ sa=0 sb=0 sd=0 m=1
.ends

.GLOBAL GND
.end
